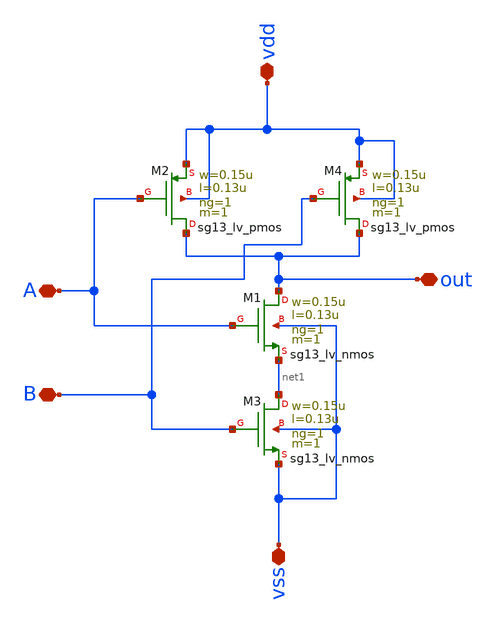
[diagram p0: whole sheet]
** sch_path: BinarytoThermo/nand_custom.sch
**.subckt nand_custom A B vdd vss out
*.iopin A
*.iopin B
*.iopin vdd
*.iopin vss
*.iopin out
XM1 out A net1 vss sg13_lv_nmos w=0.15u l=0.13u ng=1 m=1 mm_ok=1
XM2 out A vdd vdd sg13_lv_pmos w=0.15u l=0.13u ng=1 m=1 mm_ok=1
XM3 net1 B vss vss sg13_lv_nmos w=0.15u l=0.13u ng=1 m=1 mm_ok=1
XM4 out B vdd vdd sg13_lv_pmos w=0.15u l=0.13u ng=1 m=1 mm_ok=1
**.ends
.end
